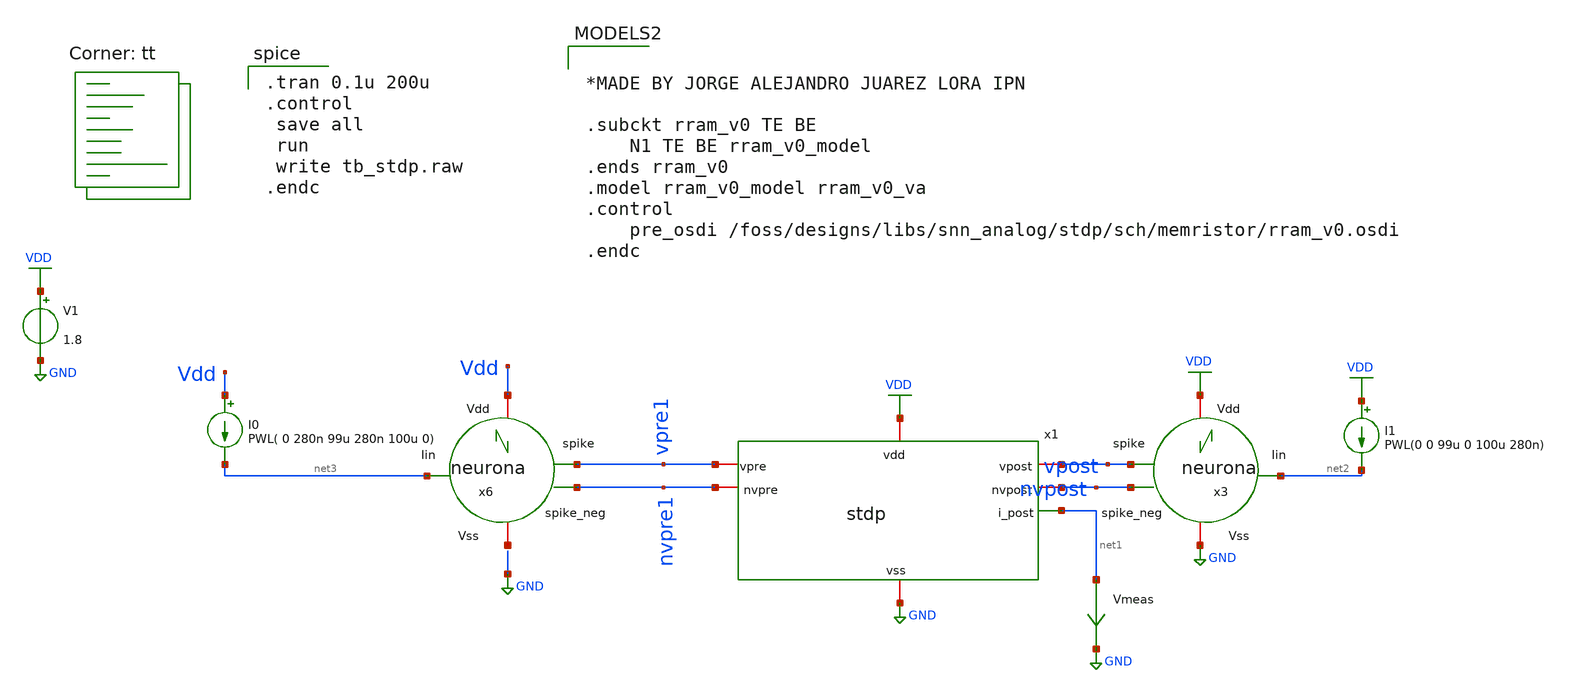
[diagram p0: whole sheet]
** sch_path: designs/libs/snn_analog/stdp/sch/tb_stdp.sch
**.subckt tb_stdp
x1 VDD GND net1 vpre1 nvpre1 nvpost vpost stdp
x3 net2 VDD GND vpost nvpost neurona
V1 VDD GND 1.8
x6 net3 Vdd net4 vpre1 nvpre1 neurona
I0 Vdd net3 PWL( 0 280n 99u 280n 100u 0)
I1 VDD net2 PWL(0 0 99u 0 100u 280n)
Vmeas net1 GND 0
.save i(vmeas)
**** begin user architecture code
.lib $::SKYWATER_MODELS/sky130.lib.spice tt

.tran 0.1u 200u
.control
 save all
 run
 write tb_stdp.raw
.endc


*MADE BY JORGE ALEJANDRO JUAREZ LORA IPN

.subckt rram_v0 TE BE
	N1 TE BE rram_v0_model
.ends rram_v0
.model rram_v0_model rram_v0_va
.control
	pre_osdi /foss/designs/libs/snn_analog/stdp/sch/memristor/rram_v0.osdi
.endc

**** end user architecture code
**.ends
.GLOBAL GND
.GLOBAL VDD
.end
